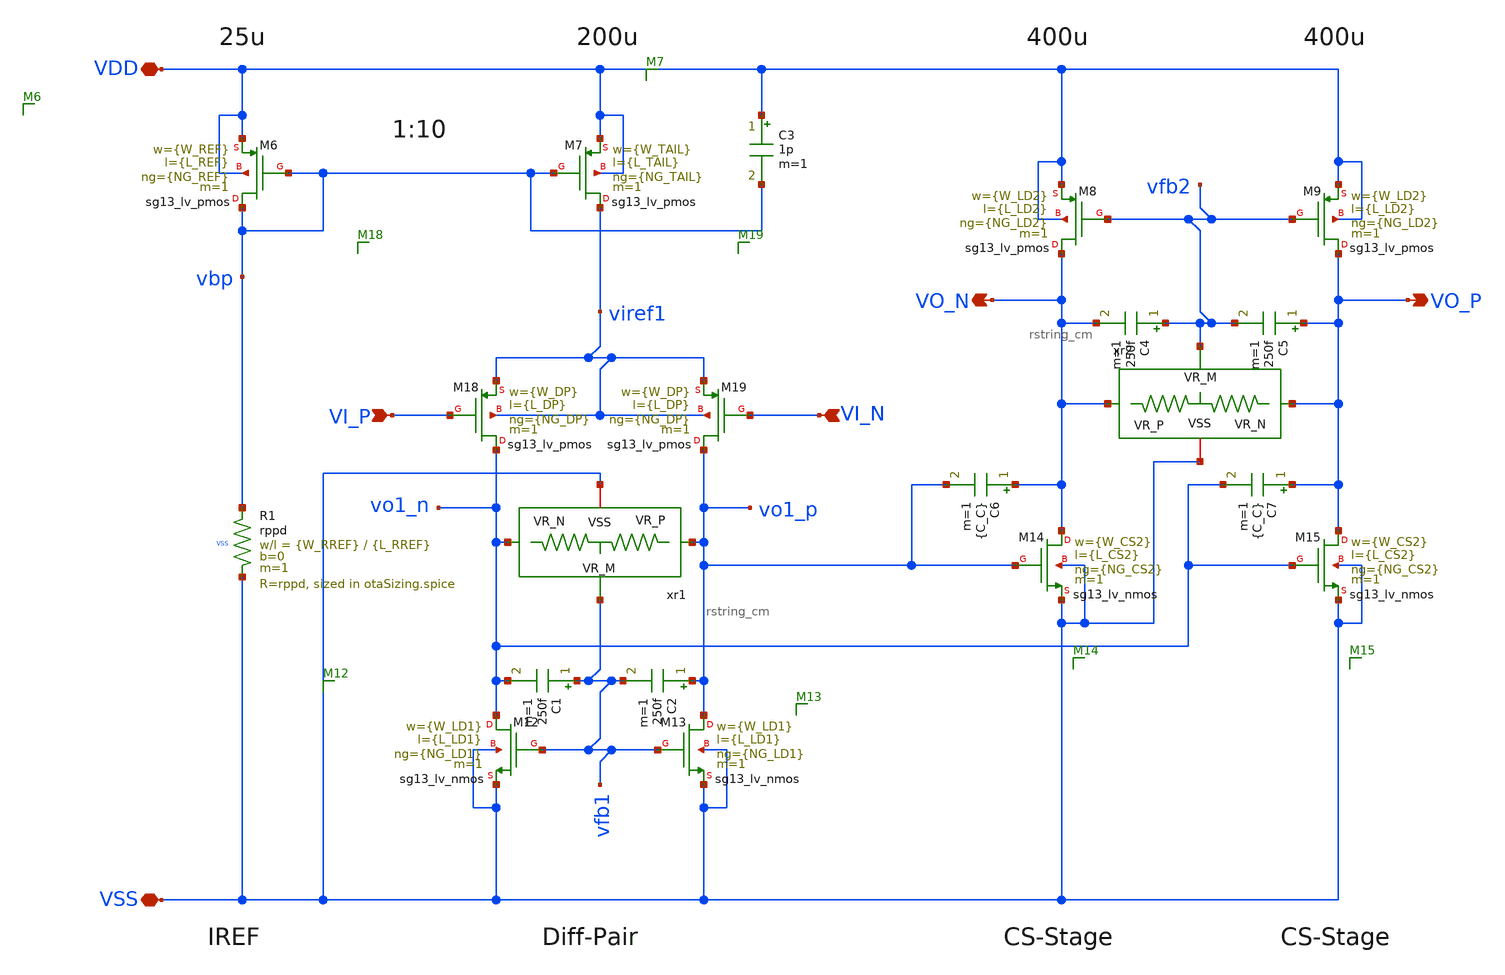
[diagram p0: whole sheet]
** sch_path: macros/filter_cmos5l/schematic/xschem/amp_no_enable_param.sch
**.subckt amp_no_enable_param VSS VDD VI_P VI_N VO_P VO_N
*.iopin VSS
*.iopin VDD
*.ipin VI_P
*.ipin VI_N
*.opin VO_P
*.opin VO_N
xr1 vfb1 vo1_n vo1_p VSS rstring_cm
xr2 vfb2 VO_P VO_N VSS rstring_cm
XM6 vbp vbp VDD VDD sg13_lv_pmos w={W_REF} l={L_REF} ng={NG_REF} m=1 mm_ok=1
XM7 viref1 vbp VDD VDD sg13_lv_pmos w={W_TAIL} l={L_TAIL} ng={NG_TAIL} m=1 mm_ok=1
XM8 VO_N vfb2 VDD VDD sg13_lv_pmos w={W_LD2} l={L_LD2} ng={NG_LD2} m=1 mm_ok=1
XM9 VO_P vfb2 VDD VDD sg13_lv_pmos w={W_LD2} l={L_LD2} ng={NG_LD2} m=1 mm_ok=1
XM12 vo1_n vfb1 VSS VSS sg13_lv_nmos w={W_LD1} l={L_LD1} ng={NG_LD1} m=1 mm_ok=1
XM13 vo1_p vfb1 VSS VSS sg13_lv_nmos w={W_LD1} l={L_LD1} ng={NG_LD1} m=1 mm_ok=1
XM14 VO_N vo1_p VSS VSS sg13_lv_nmos w={W_CS2} l={L_CS2} ng={NG_CS2} m=1 mm_ok=1
XM15 VO_P vo1_n VSS VSS sg13_lv_nmos w={W_CS2} l={L_CS2} ng={NG_CS2} m=1 mm_ok=1
XM18 vo1_n VI_P viref1 viref1 sg13_lv_pmos w={W_DP} l={L_DP} ng={NG_DP} m=1 mm_ok=1
XM19 vo1_p VI_N viref1 viref1 sg13_lv_pmos w={W_DP} l={L_DP} ng={NG_DP} m=1 mm_ok=1
XR1 vbp VSS VSS rppd w={W_RREF} l={L_RREF} m=1 b=0 mm_ok=1
C6 VO_N vo1_p {C_C} m=1
C1 vfb1 vo1_n 250f m=1
C7 VO_P vo1_n {C_C} m=1
C3 VDD vbp 1p m=1
C2 vo1_p vfb1 250f m=1
C4 vfb2 VO_N 250f m=1
C5 VO_P vfb2 250f m=1
**.ends

* expanding   symbol:  rstring_cm.sym # of pins=4
** sym_path: rstring_cm.sym
** sch_path: rstring_cm.sch
.subckt rstring_cm VR_M VR_N VR_P VSS
*.iopin VSS
*.ipin VR_P
*.ipin VR_N
*.opin VR_M
R1 VR_P VR_M 1Meg m=1
R4 VR_M VR_N 1Meg m=1
.ends

.end
